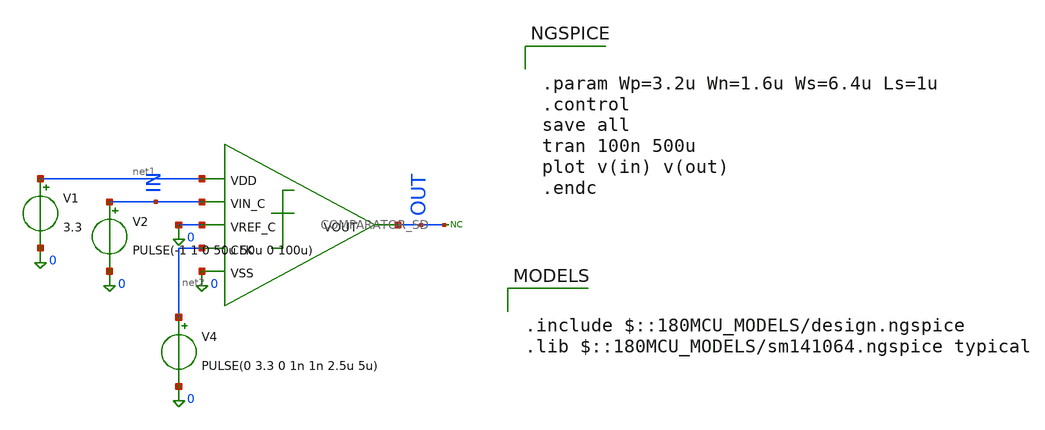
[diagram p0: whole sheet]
** sch_path: src/schematics/latched comparator/COMP_TB.sch
**.subckt COMP_TB
* noconn OUT
V2 IN 0 PULSE(-1 1 0 50u 50u 0 100u)
V4 net2 0 PULSE(0 3.3 0 1n 1n 2.5u 5u)
V1 net1 0 3.3
x1 net1 IN 0 net2 OUT 0 COMPARATOR_SD
**** begin user architecture code


.param Wp=3.2u Wn=1.6u Ws=6.4u Ls=1u
.control
save all
tran 100n 500u
plot v(in) v(out)
.endc




.include $::180MCU_MODELS/design.ngspice
.lib $::180MCU_MODELS/sm141064.ngspice typical

**** end user architecture code
**.ends

* expanding   symbol:  latched comparator/COMPARATOR_SD.sym # of pins=6
** sym_path: src/schematics/latched comparator/COMPARATOR_SD.sym
** sch_path: src/schematics/latched comparator/COMPARATOR_SD.sch
.subckt COMPARATOR_SD VDD VIN_C VREF_C CLK VOUT VSS
*.ipin VIN_C
*.ipin VREF_C
*.ipin CLK
*.opin VOUT
*.ipin VDD
*.ipin VSS
XM5 net1 VDD VDD VDD pfet_03v3 L=1u W=6.4u nf=1 ad='int((nf+1)/2) * W/nf * 0.18u' as='int((nf+2)/2) * W/nf * 0.18u'
+ pd='2*int((nf+1)/2) * (W/nf + 0.18u)' ps='2*int((nf+2)/2) * (W/nf + 0.18u)' nrd='0.18u / W' nrs='0.18u / W'
+ sa=0 sb=0 sd=0 m=1
XM1 net3 VIN_C net1 VDD pfet_03v3 L=1u W=3.2u nf=1 ad='int((nf+1)/2) * W/nf * 0.18u' as='int((nf+2)/2) * W/nf * 0.18u'
+ pd='2*int((nf+1)/2) * (W/nf + 0.18u)' ps='2*int((nf+2)/2) * (W/nf + 0.18u)' nrd='0.18u / W' nrs='0.18u / W'
+ sa=0 sb=0 sd=0 m=1
XM2 net5 VREF_C net1 VDD pfet_03v3 L=1u W=3.2u nf=1 ad='int((nf+1)/2) * W/nf * 0.18u' as='int((nf+2)/2) * W/nf * 0.18u'
+ pd='2*int((nf+1)/2) * (W/nf + 0.18u)' ps='2*int((nf+2)/2) * (W/nf + 0.18u)' nrd='0.18u / W' nrs='0.18u / W'
+ sa=0 sb=0 sd=0 m=1
XM3 net4 net2 net5 VDD pfet_03v3 L=1u W=3.2u nf=1 ad='int((nf+1)/2) * W/nf * 0.18u' as='int((nf+2)/2) * W/nf * 0.18u'
+ pd='2*int((nf+1)/2) * (W/nf + 0.18u)' ps='2*int((nf+2)/2) * (W/nf + 0.18u)' nrd='0.18u / W' nrs='0.18u / W'
+ sa=0 sb=0 sd=0 m=1
XM4 VOUT net2 net3 VDD pfet_03v3 L=1u W=3.2u nf=1 ad='int((nf+1)/2) * W/nf * 0.18u' as='int((nf+2)/2) * W/nf * 0.18u'
+ pd='2*int((nf+1)/2) * (W/nf + 0.18u)' ps='2*int((nf+2)/2) * (W/nf + 0.18u)' nrd='0.18u / W' nrs='0.18u / W'
+ sa=0 sb=0 sd=0 m=1
XM6 net2 CLK VDD VDD pfet_03v3 L=1u W=3.2u nf=1 ad='int((nf+1)/2) * W/nf * 0.18u' as='int((nf+2)/2) * W/nf * 0.18u'
+ pd='2*int((nf+1)/2) * (W/nf + 0.18u)' ps='2*int((nf+2)/2) * (W/nf + 0.18u)' nrd='0.18u / W' nrs='0.18u / W'
+ sa=0 sb=0 sd=0 m=1
XM7 net2 CLK VSS VSS nfet_03v3 L=1u W=1.6u nf=1 ad='int((nf+1)/2) * W/nf * 0.18u' as='int((nf+2)/2) * W/nf * 0.18u'
+ pd='2*int((nf+1)/2) * (W/nf + 0.18u)' ps='2*int((nf+2)/2) * (W/nf + 0.18u)' nrd='0.18u / W' nrs='0.18u / W'
+ sa=0 sb=0 sd=0 m=1
XM8 VOUT CLK net4 VSS nfet_03v3 L=1u W=1.6u nf=1 ad='int((nf+1)/2) * W/nf * 0.18u' as='int((nf+2)/2) * W/nf * 0.18u'
+ pd='2*int((nf+1)/2) * (W/nf + 0.18u)' ps='2*int((nf+2)/2) * (W/nf + 0.18u)' nrd='0.18u / W' nrs='0.18u / W'
+ sa=0 sb=0 sd=0 m=1
XM9 net7 net4 VDD VDD pfet_03v3 L=1u W=3.2u nf=1 ad='int((nf+1)/2) * W/nf * 0.18u' as='int((nf+2)/2) * W/nf * 0.18u'
+ pd='2*int((nf+1)/2) * (W/nf + 0.18u)' ps='2*int((nf+2)/2) * (W/nf + 0.18u)' nrd='0.18u / W' nrs='0.18u / W'
+ sa=0 sb=0 sd=0 m=1
XM10 VOUT CLK net7 VDD pfet_03v3 L=1u W=3.2u nf=1 ad='int((nf+1)/2) * W/nf * 0.18u' as='int((nf+2)/2) * W/nf * 0.18u'
+ pd='2*int((nf+1)/2) * (W/nf + 0.18u)' ps='2*int((nf+2)/2) * (W/nf + 0.18u)' nrd='0.18u / W' nrs='0.18u / W'
+ sa=0 sb=0 sd=0 m=1
XM11 VOUT net4 VSS VSS nfet_03v3 L=1u W=1.6u nf=1 ad='int((nf+1)/2) * W/nf * 0.18u' as='int((nf+2)/2) * W/nf * 0.18u'
+ pd='2*int((nf+1)/2) * (W/nf + 0.18u)' ps='2*int((nf+2)/2) * (W/nf + 0.18u)' nrd='0.18u / W' nrs='0.18u / W'
+ sa=0 sb=0 sd=0 m=1
XM12 net6 VOUT VDD VDD pfet_03v3 L=1u W=3.2u nf=1 ad='int((nf+1)/2) * W/nf * 0.18u' as='int((nf+2)/2) * W/nf * 0.18u'
+ pd='2*int((nf+1)/2) * (W/nf + 0.18u)' ps='2*int((nf+2)/2) * (W/nf + 0.18u)' nrd='0.18u / W' nrs='0.18u / W'
+ sa=0 sb=0 sd=0 m=1
XM13 net4 CLK net6 VDD pfet_03v3 L=1u W=3.2u nf=1 ad='int((nf+1)/2) * W/nf * 0.18u' as='int((nf+2)/2) * W/nf * 0.18u'
+ pd='2*int((nf+1)/2) * (W/nf + 0.18u)' ps='2*int((nf+2)/2) * (W/nf + 0.18u)' nrd='0.18u / W' nrs='0.18u / W'
+ sa=0 sb=0 sd=0 m=1
XM14 net4 VOUT VSS VSS nfet_03v3 L=1u W=1.6u nf=1 ad='int((nf+1)/2) * W/nf * 0.18u' as='int((nf+2)/2) * W/nf * 0.18u'
+ pd='2*int((nf+1)/2) * (W/nf + 0.18u)' ps='2*int((nf+2)/2) * (W/nf + 0.18u)' nrd='0.18u / W' nrs='0.18u / W'
+ sa=0 sb=0 sd=0 m=1
.ends

.end
